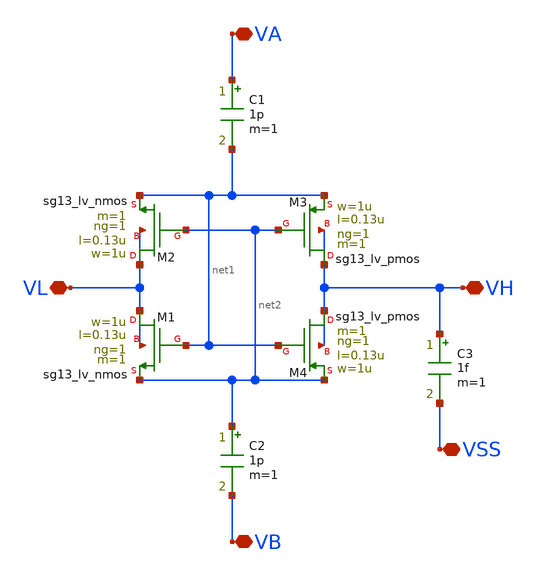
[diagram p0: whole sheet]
** sch_path: analog/core/rect_01_gen.sch
**.subckt rect_01_gen VL VH VA VB VSS
*.iopin VL
*.iopin VH
*.iopin VA
*.iopin VB
*.iopin VSS
XM1 VL net1 net2 VL sg13_lv_nmos w=1u l=0.13u ng=1 m=1 mm_ok=1
XM3 VH net2 net1 VH sg13_lv_pmos w=1u l=0.13u ng=1 m=1 mm_ok=1
XM2 VL net2 net1 VL sg13_lv_nmos w=1u l=0.13u ng=1 m=1 mm_ok=1
XM4 VH net1 net2 VH sg13_lv_pmos w=1u l=0.13u ng=1 m=1 mm_ok=1
C1 VA net1 1p m=1
C2 net2 VB 1p m=1
C3 VH VSS 1f m=1
**.ends
.end
